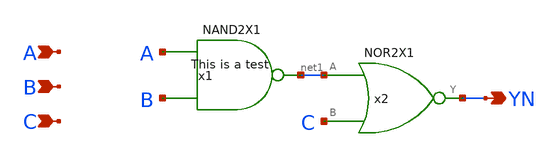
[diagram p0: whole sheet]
** sch_path: archives/lib/xschem/AOI3X1.sch
**.subckt AOI3X1 YN A B C
*.opin YN
*.ipin A
*.ipin B
*.ipin C
x1 net1 A B VDD VSS NAND2X1
x2 YN net1 C VDD VSS NOR2X1
**.ends
.end
